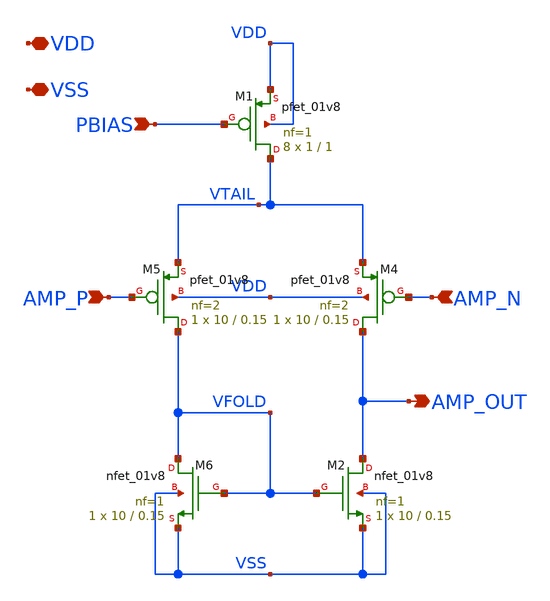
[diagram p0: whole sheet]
** sch_path: xschem/amp_p.sch
**.subckt amp_p AMP_P AMP_N AMP_OUT PBIAS VDD VSS
*.ipin AMP_P
*.ipin AMP_N
*.opin AMP_OUT
*.ipin PBIAS
*.iopin VDD
*.iopin VSS
XM1 VTAIL PBIAS VDD VDD sky130_fd_pr__pfet_01v8 L=1 W=1 nf=1 ad='int((nf+1)/2) * W/nf * 0.29' as='int((nf+2)/2) * W/nf * 0.29'
+ pd='2*int((nf+1)/2) * (W/nf + 0.29)' ps='2*int((nf+2)/2) * (W/nf + 0.29)' nrd='0.29 / W' nrs='0.29 / W'
+ sa=0 sb=0 sd=0 mult=8 m=8
XM2 AMP_OUT VFOLD VSS VSS sky130_fd_pr__nfet_01v8 L=0.15 W=10 nf=1 ad='int((nf+1)/2) * W/nf * 0.29' as='int((nf+2)/2) * W/nf * 0.29'
+ pd='2*int((nf+1)/2) * (W/nf + 0.29)' ps='2*int((nf+2)/2) * (W/nf + 0.29)' nrd='0.29 / W' nrs='0.29 / W'
+ sa=0 sb=0 sd=0 mult=1 m=1
XM6 VFOLD VFOLD VSS VSS sky130_fd_pr__nfet_01v8 L=0.15 W=10 nf=1 ad='int((nf+1)/2) * W/nf * 0.29' as='int((nf+2)/2) * W/nf * 0.29'
+ pd='2*int((nf+1)/2) * (W/nf + 0.29)' ps='2*int((nf+2)/2) * (W/nf + 0.29)' nrd='0.29 / W' nrs='0.29 / W'
+ sa=0 sb=0 sd=0 mult=1 m=1
XM4 AMP_OUT AMP_N VTAIL VDD sky130_fd_pr__pfet_01v8 L=0.15 W=10 nf=2 ad='int((nf+1)/2) * W/nf * 0.29'
+ as='int((nf+2)/2) * W/nf * 0.29' pd='2*int((nf+1)/2) * (W/nf + 0.29)' ps='2*int((nf+2)/2) * (W/nf + 0.29)'
+ nrd='0.29 / W' nrs='0.29 / W' sa=0 sb=0 sd=0 mult=1 m=1
XM5 VFOLD AMP_P VTAIL VDD sky130_fd_pr__pfet_01v8 L=0.15 W=10 nf=2 ad='int((nf+1)/2) * W/nf * 0.29' as='int((nf+2)/2) * W/nf * 0.29'
+ pd='2*int((nf+1)/2) * (W/nf + 0.29)' ps='2*int((nf+2)/2) * (W/nf + 0.29)' nrd='0.29 / W' nrs='0.29 / W'
+ sa=0 sb=0 sd=0 mult=1 m=1
**.ends
.end
